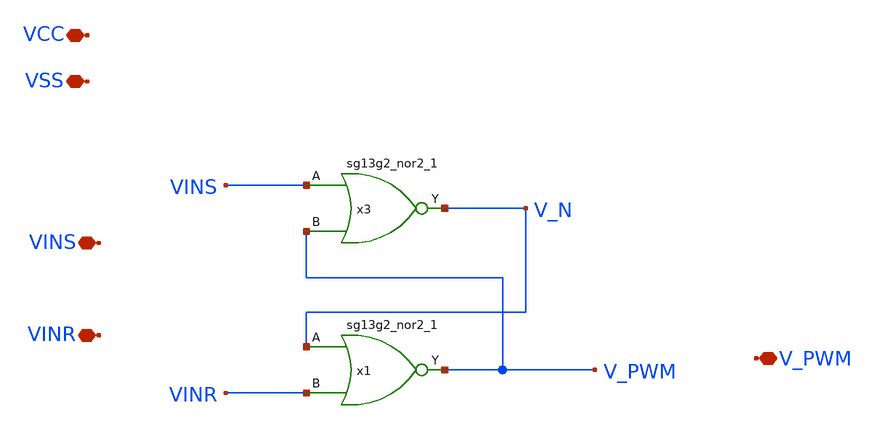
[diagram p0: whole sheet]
** sch_path: ChipUSM_AnalogTrack24/SR_Latch_NOR.sch
* IHP-GmbH/IHP-Open-PDK/ihp-sg13g2/libs.tech/xschem/sg13g2_stdcells/sg13g2_nor2_1.sch:
* Copyright 2023 IHP PDK Authors
* Licensed under the Apache License, Version 2.0 (the "License");
**.subckt SR_Latch_NOR VINS V_PWM VCC VSS VINR
*.iopin VINS
*.iopin V_PWM
*.iopin VCC
*.iopin VSS
*.iopin VINR
x3 V_N VINS V_PWM VCC VSS sg13g2_nor2_1
x1 V_PWM V_N VINR VCC VSS sg13g2_nor2_1
**.ends

* expanding   symbol:  sg13g2_stdcells/sg13g2_nor2_1.sym # of pins=3
** sym_path: sg13g2_stdcells/sg13g2_nor2_1.sym
** sch_path: sg13g2_stdcells/sg13g2_nor2_1.sch
.subckt sg13g2_nor2_1 Y A B VDD VSS
*.opin Y
*.ipin B
*.ipin A
*.iopin VDD
*.iopin VSS
XM1 Y A VSS VSS sg13_lv_nmos w=740.00n l=130.00n ng=1 m=1 mm_ok=1
XM2 Y B VSS VSS sg13_lv_nmos w=740.00n l=130.00n ng=1 m=1 mm_ok=1
XM3 net1 A VDD VDD sg13_lv_pmos w=1.12u l=130.00n ng=1 m=1 mm_ok=1
XM4 Y B net1 VDD sg13_lv_pmos w=1.12u l=130.00n ng=1 m=1 mm_ok=1
.ends

.end
